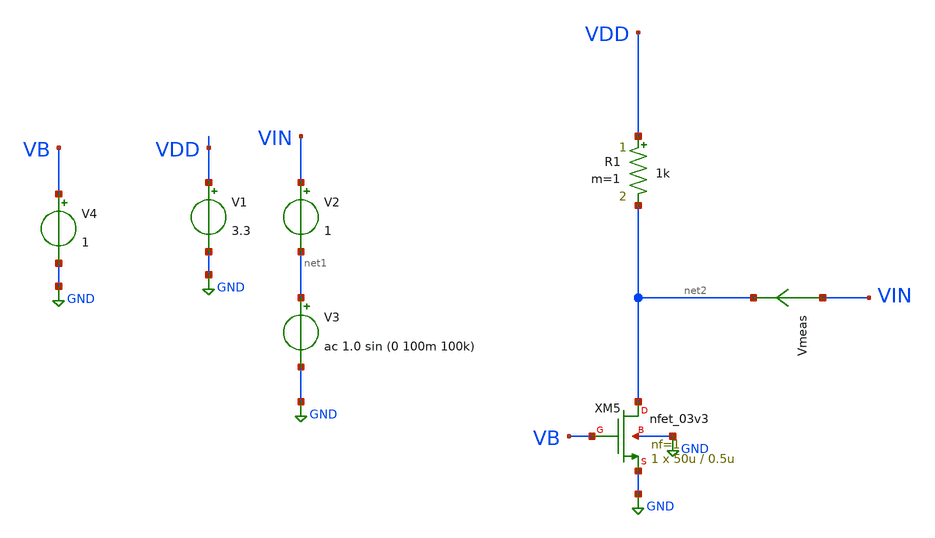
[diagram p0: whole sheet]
** sch_path: output_impedance/output_impedance1.sch
**.subckt output_impedance1
V1 VDD GND 3.3
V2 VIN net1 1
V4 VB GND 1
XM5 net2 VB GND GND nfet_03v3 L=0.5u W=50u nf=1 ad='int((nf+1)/2) * W/nf * 0.18u' as='int((nf+2)/2) * W/nf * 0.18u'
+ pd='2*int((nf+1)/2) * (W/nf + 0.18u)' ps='2*int((nf+2)/2) * (W/nf + 0.18u)' nrd='0.18u / W' nrs='0.18u / W'
+ sa=0 sb=0 sd=0 m=1
Vmeas VIN net2 0
.save i(vmeas)
R1 VDD net2 1k m=1
V3 net1 GND ac 1.0 sin (0 100m 100k)
**** begin user architecture code

.include $::180MCU_MODELS/design.ngspice
*.lib $::180MCU_MODELS/sm141064.ngspice statistical
*.lib $::180MCU_MODELS/sm141064.ngspice res_statistical
.lib $::180MCU_MODELS/sm141064.ngspice typical
.lib $::180MCU_MODELS/sm141064.ngspice res_typical
.lib $::180MCU_MODELS/sm141064.ngspice moscap_typical
.lib $::180MCU_MODELS/sm141064.ngspice bjt_typical
.lib $::180MCU_MODELS/sm141064.ngspice diode_typical
.lib $::180MCU_MODELS/sm141064.ngspice mimcap_typical
.TEMP 27

.param   sw_stat_global = 1   sw_stat_mism = 1  mc_skew = 3  res_mc_skew = 3  cap_mc_skew = 3
+  fnoicor = 1



.control
save all
dc V2 0 3.3 0.01

plot i(Vmeas) 1/(deriv(i(Vmeas)))
plot i(Vmeas)
plot deriv(v(VOUT))
tran 100n 10u
plot i(Vmeas)
.endc

**** end user architecture code
**.ends
.GLOBAL GND
.end
